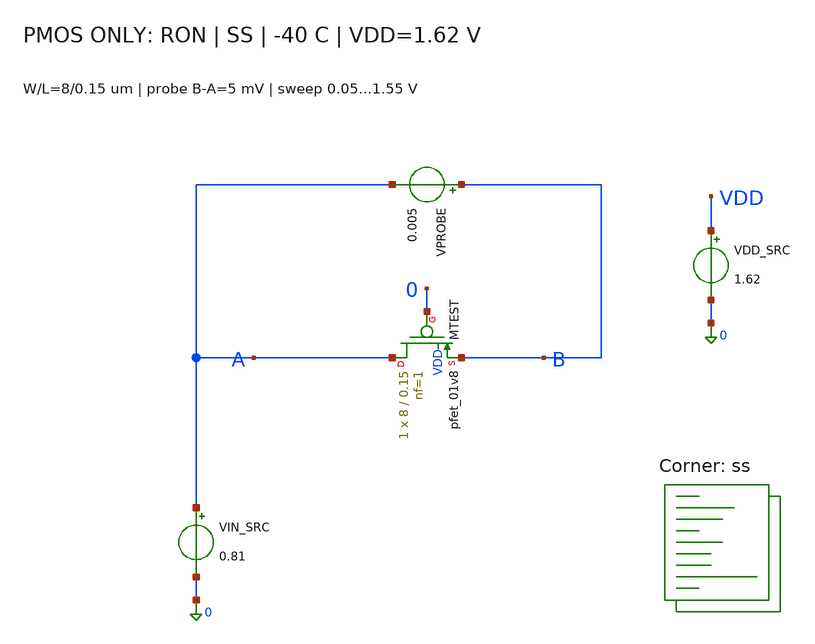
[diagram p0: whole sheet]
** sch_path: blocks/05_Switch_Network/sim/tb_5B_ron_pmos.sch
**.subckt tb_5B_ron_pmos
VPROBE B A 0.005
.save i(vprobe)
VIN_SRC A 0 0.81
VDD_SRC VDD 0 1.62
XMTEST A 0 B VDD sky130_fd_pr__pfet_01v8 L=0.15 W=8 nf=1 ad=2.32 as=2.32 pd=16.58 ps=16.58
+ nrd=0.03625 nrs=0.03625 sa=0 sb=0 sd=0 mult=1 m=1
**** begin user architecture code
.lib $::SKYWATER_MODELS/sky130.lib.spice ss


.option scale=1e-6 reltol=1e-5 abstol=1e-14 vntol=1e-8
.temp -40
.control
save all
set wr_singlescale
set wr_vecnames
set numdgt=15
dc VIN_SRC 0.05 1.55 0.005
let RON=abs((v(B)-v(A))/i(VPROBE))
meas dc RON_MIN MIN RON
meas dc RON_MAX MAX RON
meas dc RON_060 FIND RON AT=0.6
meas dc RON_081 FIND RON AT=0.81
meas dc RON_089 FIND RON AT=0.89
meas dc RON_090 FIND RON AT=0.9
meas dc RON_120 FIND RON AT=1.2
wrdata ron_pmos_ss_1p62_m40.dat v(A) v(B) i(VPROBE) RON
plot RON
.endc


**** end user architecture code
**.ends
.end
